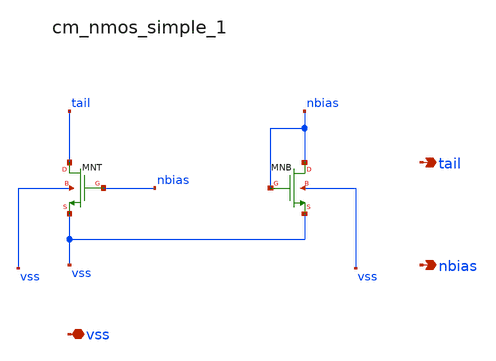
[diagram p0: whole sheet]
** sch_path: analog-db/raw/ldo_009_fer_5t_pass/hier/blocks/cm_nmos_simple_1.sch
**.subckt cm_nmos_simple_1 vss tail nbias
*.iopin vss
*.opin tail
*.opin nbias
XMNB nbias nbias vss vss sg13_lv_nmos w=x_dut_xmnb_w l=x_dut_xmnb_l ng=1 m=x_dut_xmnb_m
XMNT tail nbias vss vss sg13_lv_nmos w=x_dut_xmnt_w l=x_dut_xmnt_l ng=1 m=x_dut_xmnt_m
**.ends
.end
